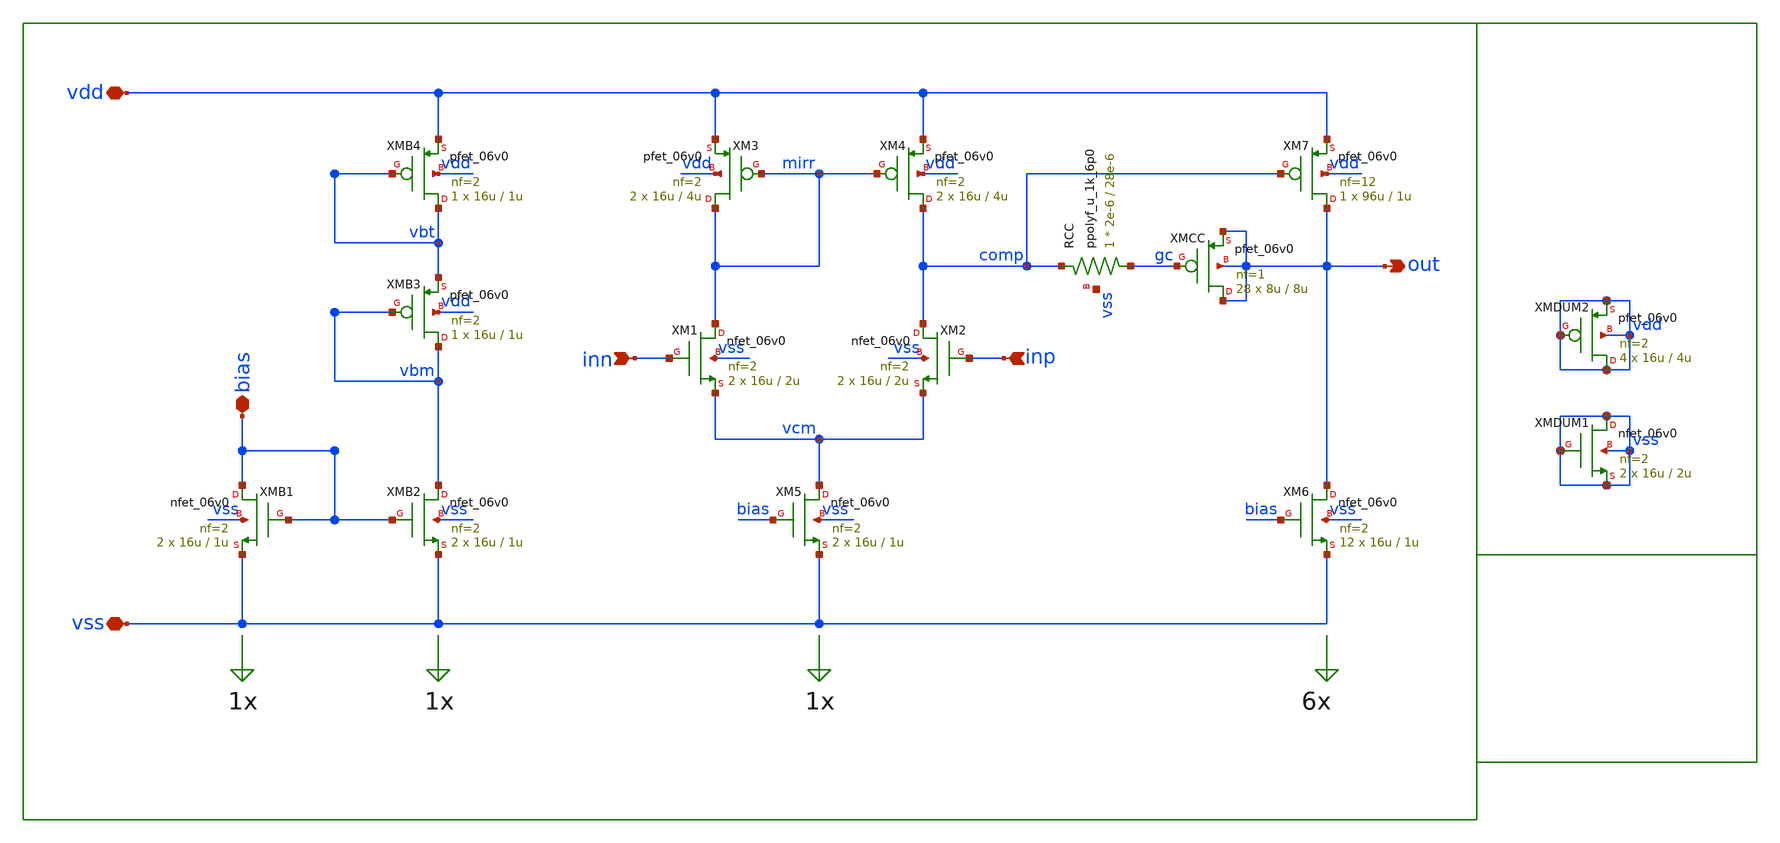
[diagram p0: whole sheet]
** sch_path: xschem/sch/testbuffer/tb_amplifier/tb_amplifier.sch
**.subckt tb_amplifier inn inp out bias vdd vss
*.ipin inn
*.ipin inp
*.opin out
*.iopin bias
*.iopin vdd
*.iopin vss
XM3 mirr mirr vdd vdd pfet_06v0 L=4u W=16u nf=2 ad='int((nf+1)/2) * W/nf * 0.18u' as='int((nf+2)/2) * W/nf * 0.18u'
+ pd='2*int((nf+1)/2) * (W/nf + 0.18u)' ps='2*int((nf+2)/2) * (W/nf + 0.18u)' nrd='0.18u / W' nrs='0.18u / W'
+ sa=0 sb=0 sd=0 m=2
XM4 comp mirr vdd vdd pfet_06v0 L=4u W=16u nf=2 ad='int((nf+1)/2) * W/nf * 0.18u' as='int((nf+2)/2) * W/nf * 0.18u'
+ pd='2*int((nf+1)/2) * (W/nf + 0.18u)' ps='2*int((nf+2)/2) * (W/nf + 0.18u)' nrd='0.18u / W' nrs='0.18u / W'
+ sa=0 sb=0 sd=0 m=2
XM2 comp inp vcm vss nfet_06v0 L=2u W=16u nf=2 ad='int((nf+1)/2) * W/nf * 0.18u' as='int((nf+2)/2) * W/nf * 0.18u'
+ pd='2*int((nf+1)/2) * (W/nf + 0.18u)' ps='2*int((nf+2)/2) * (W/nf + 0.18u)' nrd='0.18u / W' nrs='0.18u / W'
+ sa=0 sb=0 sd=0 m=2
XM1 mirr inn vcm vss nfet_06v0 L=2u W=16u nf=2 ad='int((nf+1)/2) * W/nf * 0.18u' as='int((nf+2)/2) * W/nf * 0.18u'
+ pd='2*int((nf+1)/2) * (W/nf + 0.18u)' ps='2*int((nf+2)/2) * (W/nf + 0.18u)' nrd='0.18u / W' nrs='0.18u / W'
+ sa=0 sb=0 sd=0 m=2
XM5 vcm bias vss vss nfet_06v0 L=1u W=16u nf=2 ad='int((nf+1)/2) * W/nf * 0.18u' as='int((nf+2)/2) * W/nf * 0.18u'
+ pd='2*int((nf+1)/2) * (W/nf + 0.18u)' ps='2*int((nf+2)/2) * (W/nf + 0.18u)' nrd='0.18u / W' nrs='0.18u / W'
+ sa=0 sb=0 sd=0 m=2
XM6 out bias vss vss nfet_06v0 L=1u W=16u nf=2 ad='int((nf+1)/2) * W/nf * 0.18u' as='int((nf+2)/2) * W/nf * 0.18u'
+ pd='2*int((nf+1)/2) * (W/nf + 0.18u)' ps='2*int((nf+2)/2) * (W/nf + 0.18u)' nrd='0.18u / W' nrs='0.18u / W'
+ sa=0 sb=0 sd=0 m=12
XM7 out comp vdd vdd pfet_06v0 L=1u W=96u nf=12 ad='int((nf+1)/2) * W/nf * 0.18u' as='int((nf+2)/2) * W/nf * 0.18u'
+ pd='2*int((nf+1)/2) * (W/nf + 0.18u)' ps='2*int((nf+2)/2) * (W/nf + 0.18u)' nrd='0.18u / W' nrs='0.18u / W'
+ sa=0 sb=0 sd=0 m=1
XMB1 bias bias vss vss nfet_06v0 L=1u W=16u nf=2 ad='int((nf+1)/2) * W/nf * 0.18u' as='int((nf+2)/2) * W/nf * 0.18u'
+ pd='2*int((nf+1)/2) * (W/nf + 0.18u)' ps='2*int((nf+2)/2) * (W/nf + 0.18u)' nrd='0.18u / W' nrs='0.18u / W'
+ sa=0 sb=0 sd=0 m=2
XMB2 vbm bias vss vss nfet_06v0 L=1u W=16u nf=2 ad='int((nf+1)/2) * W/nf * 0.18u' as='int((nf+2)/2) * W/nf * 0.18u'
+ pd='2*int((nf+1)/2) * (W/nf + 0.18u)' ps='2*int((nf+2)/2) * (W/nf + 0.18u)' nrd='0.18u / W' nrs='0.18u / W'
+ sa=0 sb=0 sd=0 m=2
XMB3 vbm vbm vbt vdd pfet_06v0 L=1u W=16u nf=2 ad='int((nf+1)/2) * W/nf * 0.18u' as='int((nf+2)/2) * W/nf * 0.18u'
+ pd='2*int((nf+1)/2) * (W/nf + 0.18u)' ps='2*int((nf+2)/2) * (W/nf + 0.18u)' nrd='0.18u / W' nrs='0.18u / W'
+ sa=0 sb=0 sd=0 m=1
XMB4 vbt vbt vdd vdd pfet_06v0 L=1u W=16u nf=2 ad='int((nf+1)/2) * W/nf * 0.18u' as='int((nf+2)/2) * W/nf * 0.18u'
+ pd='2*int((nf+1)/2) * (W/nf + 0.18u)' ps='2*int((nf+2)/2) * (W/nf + 0.18u)' nrd='0.18u / W' nrs='0.18u / W'
+ sa=0 sb=0 sd=0 m=1
XRCC gc comp vss ppolyf_u_1k_6p0 r_width=2e-6 r_length=28e-6 m=1
XMCC out gc out out pfet_06v0 L=8u W=8u nf=1 ad='int((nf+1)/2) * W/nf * 0.18u' as='int((nf+2)/2) * W/nf * 0.18u'
+ pd='2*int((nf+1)/2) * (W/nf + 0.18u)' ps='2*int((nf+2)/2) * (W/nf + 0.18u)' nrd='0.18u / W' nrs='0.18u / W'
+ sa=0 sb=0 sd=0 m=28
XMDUM1 vss vss vss vss nfet_06v0 L=2u W=16u nf=2 ad='int((nf+1)/2) * W/nf * 0.18u' as='int((nf+2)/2) * W/nf * 0.18u'
+ pd='2*int((nf+1)/2) * (W/nf + 0.18u)' ps='2*int((nf+2)/2) * (W/nf + 0.18u)' nrd='0.18u / W' nrs='0.18u / W'
+ sa=0 sb=0 sd=0 m=2
XMDUM2 vdd vdd vdd vdd pfet_06v0 L=4u W=16u nf=2 ad='int((nf+1)/2) * W/nf * 0.18u' as='int((nf+2)/2) * W/nf * 0.18u'
+ pd='2*int((nf+1)/2) * (W/nf + 0.18u)' ps='2*int((nf+2)/2) * (W/nf + 0.18u)' nrd='0.18u / W' nrs='0.18u / W'
+ sa=0 sb=0 sd=0 m=4
**.ends
.end
